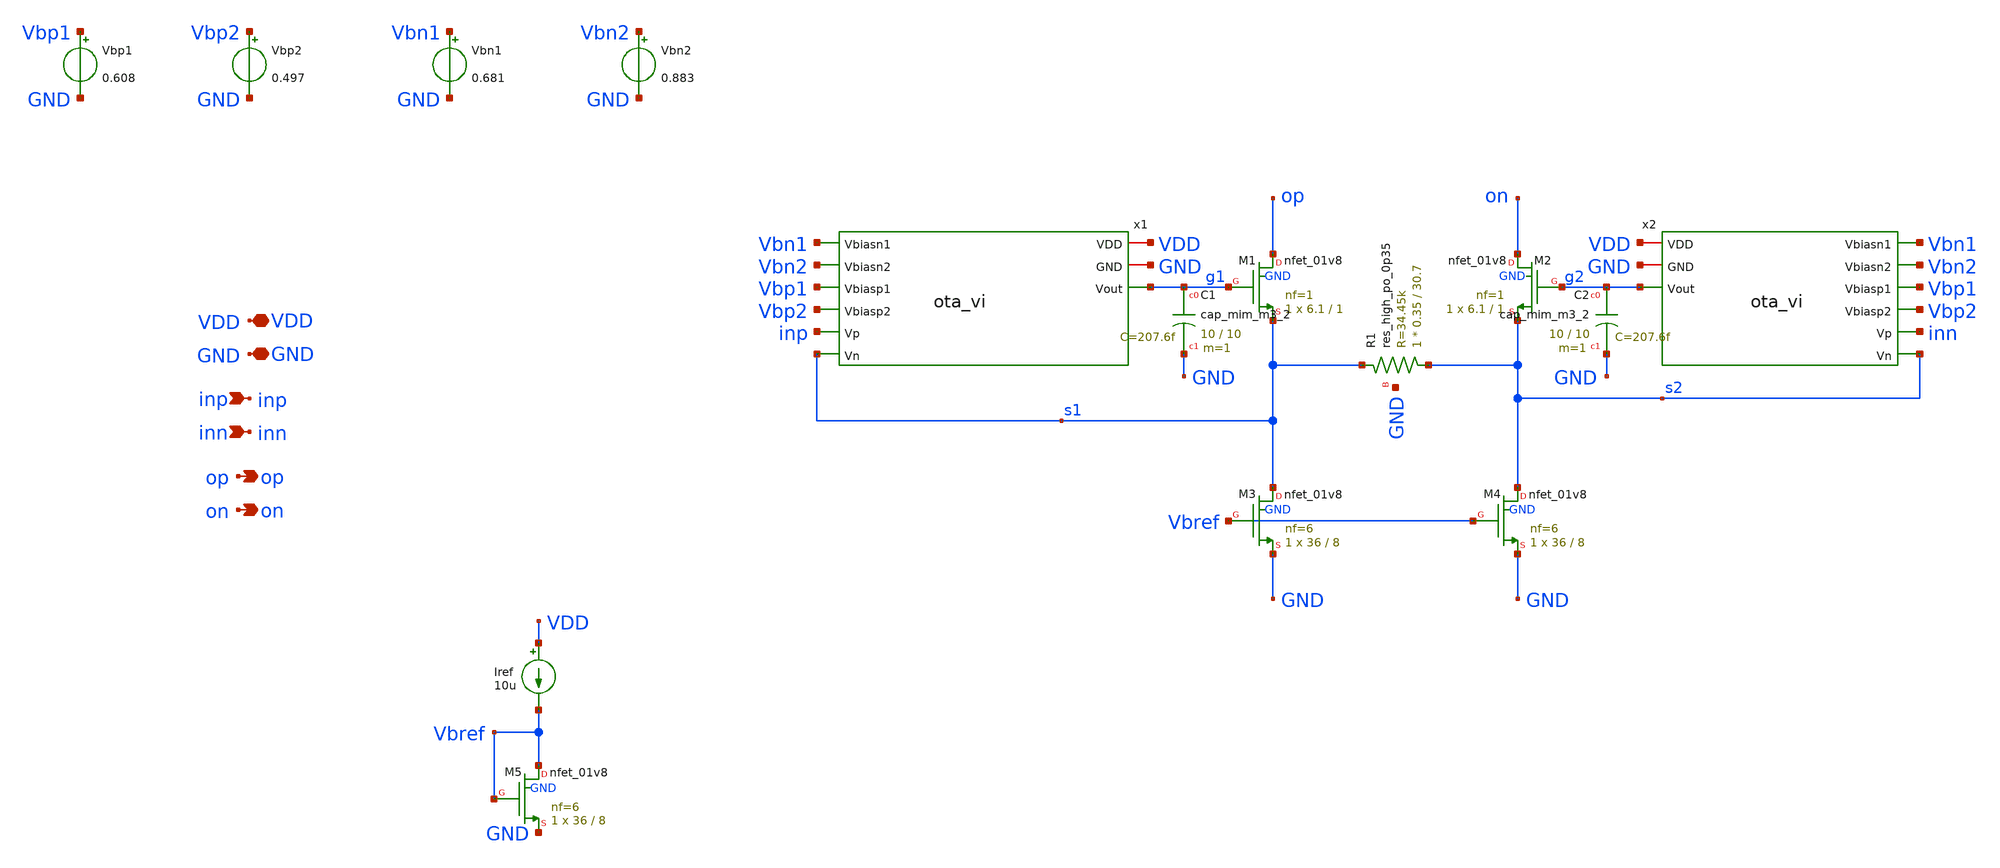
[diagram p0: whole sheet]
** sch_path: sch/vi_converter/vi_converter.sch
**.subckt vi_converter inp op VDD GND inn on
*.ipin inp
*.opin op
*.iopin VDD
*.iopin GND
*.ipin inn
*.opin on
x1 VDD GND Vbn1 Vbn2 Vbp1 Vbp2 inp s1 g1 ota_vi
XM1 op g1 s1 GND sky130_fd_pr__nfet_01v8 L=1 W=6.1 nf=1 ad='int((1 + 1)/2) * 6.1 / 1 * 0.29' as='int((1 + 2)/2) * 6.1 / 1 * 0.29'
+ pd='2*int((1 + 1)/2) * (6.1 / 1 + 0.29)' ps='2*int((1 + 2)/2) * (6.1 / 1 + 0.29)' nrd='0.29 / 6.1 ' nrs='0.29 / 6.1 '
+ sa=0 sb=0 sd=0 mult=1 m=1
XM2 on g2 s2 GND sky130_fd_pr__nfet_01v8 L=1 W=6.1 nf=1 ad='int((1 + 1)/2) * 6.1 / 1 * 0.29' as='int((1 + 2)/2) * 6.1 / 1 * 0.29'
+ pd='2*int((1 + 1)/2) * (6.1 / 1 + 0.29)' ps='2*int((1 + 2)/2) * (6.1 / 1 + 0.29)' nrd='0.29 / 6.1 ' nrs='0.29 / 6.1 '
+ sa=0 sb=0 sd=0 mult=1 m=1
XM3 s1 Vbref GND GND sky130_fd_pr__nfet_01v8 L=8 W=36 nf=6 ad='int((6 + 1)/2) * 36 / 6 * 0.29' as='int((6 + 2)/2) * 36 / 6 * 0.29'
+ pd='2*int((6 + 1)/2) * (36 / 6 + 0.29)' ps='2*int((6 + 2)/2) * (36 / 6 + 0.29)' nrd='0.29 / 36 ' nrs='0.29 / 36 '
+ sa=0 sb=0 sd=0 mult=1 m=1
XM4 s2 Vbref GND GND sky130_fd_pr__nfet_01v8 L=8 W=36 nf=6 ad='int((6 + 1)/2) * 36 / 6 * 0.29' as='int((6 + 2)/2) * 36 / 6 * 0.29'
+ pd='2*int((6 + 1)/2) * (36 / 6 + 0.29)' ps='2*int((6 + 2)/2) * (36 / 6 + 0.29)' nrd='0.29 / 36 ' nrs='0.29 / 36 '
+ sa=0 sb=0 sd=0 mult=1 m=1
Iref VDD Vbref 10u
XC1 g1 GND sky130_fd_pr__cap_mim_m3_2 W=10 L=10 MF=1 m=1
x2 VDD GND Vbn1 Vbn2 Vbp1 Vbp2 inn s2 g2 ota_vi
XC2 g2 GND sky130_fd_pr__cap_mim_m3_2 W=10 L=10 MF=1 m=1
XR1 s2 s1 GND sky130_fd_pr__res_high_po_0p35 L=30.7 mult=1 m=1
Vbp2 Vbp2 GND 0.497
.save i(vbp2)
Vbp1 Vbp1 GND 0.608
.save i(vbp1)
Vbn1 Vbn1 GND 0.681
.save i(vbn1)
Vbn2 Vbn2 GND 0.883
.save i(vbn2)
XM5 Vbref Vbref GND GND sky130_fd_pr__nfet_01v8 L=8 W=36 nf=6 ad='int((6 + 1)/2) * 36 / 6 * 0.29' as='int((6 + 2)/2) * 36 / 6 * 0.29'
+ pd='2*int((6 + 1)/2) * (36 / 6 + 0.29)' ps='2*int((6 + 2)/2) * (36 / 6 + 0.29)' nrd='0.29 / 36 ' nrs='0.29 / 36 '
+ sa=0 sb=0 sd=0 mult=1 m=1
**.ends

* expanding   symbol:  vi_converter/ota_vi.sym # of pins=9
** sym_path: sch/vi_converter/ota_vi.sym
** sch_path: sch/vi_converter/ota_vi.sch
.subckt ota_vi VDD GND Vbiasn1 Vbiasn2 Vbiasp1 Vbiasp2 Vp Vn Vout
*.ipin Vbiasn2
*.opin Vout
*.iopin VDD
*.iopin GND
*.ipin Vp
*.ipin Vn
*.ipin Vbiasp1
*.ipin Vbiasp2
*.ipin Vbiasn1
XM3 net4 Vbiasn2 net3 GND sky130_fd_pr__nfet_01v8 L=1 W=4.6 nf=1 ad='int((1 + 1)/2) * 4.6 / 1 * 0.29'
+ as='int((1 + 2)/2) * 4.6 / 1 * 0.29' pd='2*int((1 + 1)/2) * (4.6 / 1 + 0.29)' ps='2*int((1 + 2)/2) * (4.6 / 1 + 0.29)'
+ nrd='0.29 / 4.6 ' nrs='0.29 / 4.6 ' sa=0 sb=0 sd=0 mult=1 m=1
XM4 Vout Vbiasn2 net2 GND sky130_fd_pr__nfet_01v8 L=1 W=4.6 nf=1 ad='int((1 + 1)/2) * 4.6 / 1 * 0.29'
+ as='int((1 + 2)/2) * 4.6 / 1 * 0.29' pd='2*int((1 + 1)/2) * (4.6 / 1 + 0.29)' ps='2*int((1 + 2)/2) * (4.6 / 1 + 0.29)'
+ nrd='0.29 / 4.6 ' nrs='0.29 / 4.6 ' sa=0 sb=0 sd=0 mult=1 m=1
XM5 net3 Vbiasn1 GND GND sky130_fd_pr__nfet_01v8 L=2 W=12 nf=2 ad='int((2 + 1)/2) * 12 / 2 * 0.29' as='int((2 + 2)/2) * 12 / 2 * 0.29'
+ pd='2*int((2 + 1)/2) * (12 / 2 + 0.29)' ps='2*int((2 + 2)/2) * (12 / 2 + 0.29)' nrd='0.29 / 12 ' nrs='0.29 / 12 '
+ sa=0 sb=0 sd=0 mult=1 m=1
XM6 net2 Vbiasn1 GND GND sky130_fd_pr__nfet_01v8 L=2 W=12 nf=2 ad='int((2 + 1)/2) * 12 / 2 * 0.29' as='int((2 + 2)/2) * 12 / 2 * 0.29'
+ pd='2*int((2 + 1)/2) * (12 / 2 + 0.29)' ps='2*int((2 + 2)/2) * (12 / 2 + 0.29)' nrd='0.29 / 12 ' nrs='0.29 / 12 '
+ sa=0 sb=0 sd=0 mult=1 m=1
XM7 net4 Vbiasp2 net5 VDD sky130_fd_pr__pfet_01v8 L=1 W=15.6 nf=3 ad='int((3 + 1)/2) * 15.6 / 3 * 0.29'
+ as='int((3 + 2)/2) * 15.6 / 3 * 0.29' pd='2*int((3 + 1)/2) * (15.6 / 3 + 0.29)' ps='2*int((3 + 2)/2) * (15.6 / 3 + 0.29)'
+ nrd='0.29 / 15.6 ' nrs='0.29 / 15.6 ' sa=0 sb=0 sd=0 mult=1 m=1
XM8 Vout Vbiasp2 net6 VDD sky130_fd_pr__pfet_01v8 L=1 W=15.6 nf=3 ad='int((3 + 1)/2) * 15.6 / 3 * 0.29'
+ as='int((3 + 2)/2) * 15.6 / 3 * 0.29' pd='2*int((3 + 1)/2) * (15.6 / 3 + 0.29)' ps='2*int((3 + 2)/2) * (15.6 / 3 + 0.29)'
+ nrd='0.29 / 15.6 ' nrs='0.29 / 15.6 ' sa=0 sb=0 sd=0 mult=1 m=1
XM9 net5 net4 VDD VDD sky130_fd_pr__pfet_01v8 L=2 W=22.6 nf=4 ad='int((4 + 1)/2) * 22.6 / 4 * 0.29' as='int((4 + 2)/2) * 22.6 / 4 * 0.29'
+ pd='2*int((4 + 1)/2) * (22.6 / 4 + 0.29)' ps='2*int((4 + 2)/2) * (22.6 / 4 + 0.29)' nrd='0.29 / 22.6 '
+ nrs='0.29 / 22.6 ' sa=0 sb=0 sd=0 mult=1 m=1
XM10 net6 net4 VDD VDD sky130_fd_pr__pfet_01v8 L=2 W=22.6 nf=4 ad='int((4 + 1)/2) * 22.6 / 4 * 0.29'
+ as='int((4 + 2)/2) * 22.6 / 4 * 0.29' pd='2*int((4 + 1)/2) * (22.6 / 4 + 0.29)' ps='2*int((4 + 2)/2) * (22.6 / 4 + 0.29)'
+ nrd='0.29 / 22.6 ' nrs='0.29 / 22.6 ' sa=0 sb=0 sd=0 mult=1 m=1
XM11 net1 Vbiasp1 VDD VDD sky130_fd_pr__pfet_01v8 L=2 W=17.7 nf=3 ad='int((3 + 1)/2) * 17.7 / 3 * 0.29'
+ as='int((3 + 2)/2) * 17.7 / 3 * 0.29' pd='2*int((3 + 1)/2) * (17.7 / 3 + 0.29)' ps='2*int((3 + 2)/2) * (17.7 / 3 + 0.29)'
+ nrd='0.29 / 17.7 ' nrs='0.29 / 17.7 ' sa=0 sb=0 sd=0 mult=1 m=1
XM1 net3 Vp net1 VDD sky130_fd_pr__pfet_01v8_lvt L=1 W=14.6 nf=2 ad='int((2 + 1)/2) * 14.6 / 2 * 0.29'
+ as='int((2 + 2)/2) * 14.6 / 2 * 0.29' pd='2*int((2 + 1)/2) * (14.6 / 2 + 0.29)' ps='2*int((2 + 2)/2) * (14.6 / 2 + 0.29)'
+ nrd='0.29 / 14.6 ' nrs='0.29 / 14.6 ' sa=0 sb=0 sd=0 mult=1 m=1
XM2 net2 Vn net1 VDD sky130_fd_pr__pfet_01v8_lvt L=1 W=14.6 nf=2 ad='int((2 + 1)/2) * 14.6 / 2 * 0.29'
+ as='int((2 + 2)/2) * 14.6 / 2 * 0.29' pd='2*int((2 + 1)/2) * (14.6 / 2 + 0.29)' ps='2*int((2 + 2)/2) * (14.6 / 2 + 0.29)'
+ nrd='0.29 / 14.6 ' nrs='0.29 / 14.6 ' sa=0 sb=0 sd=0 mult=1 m=1
.ends

.end
